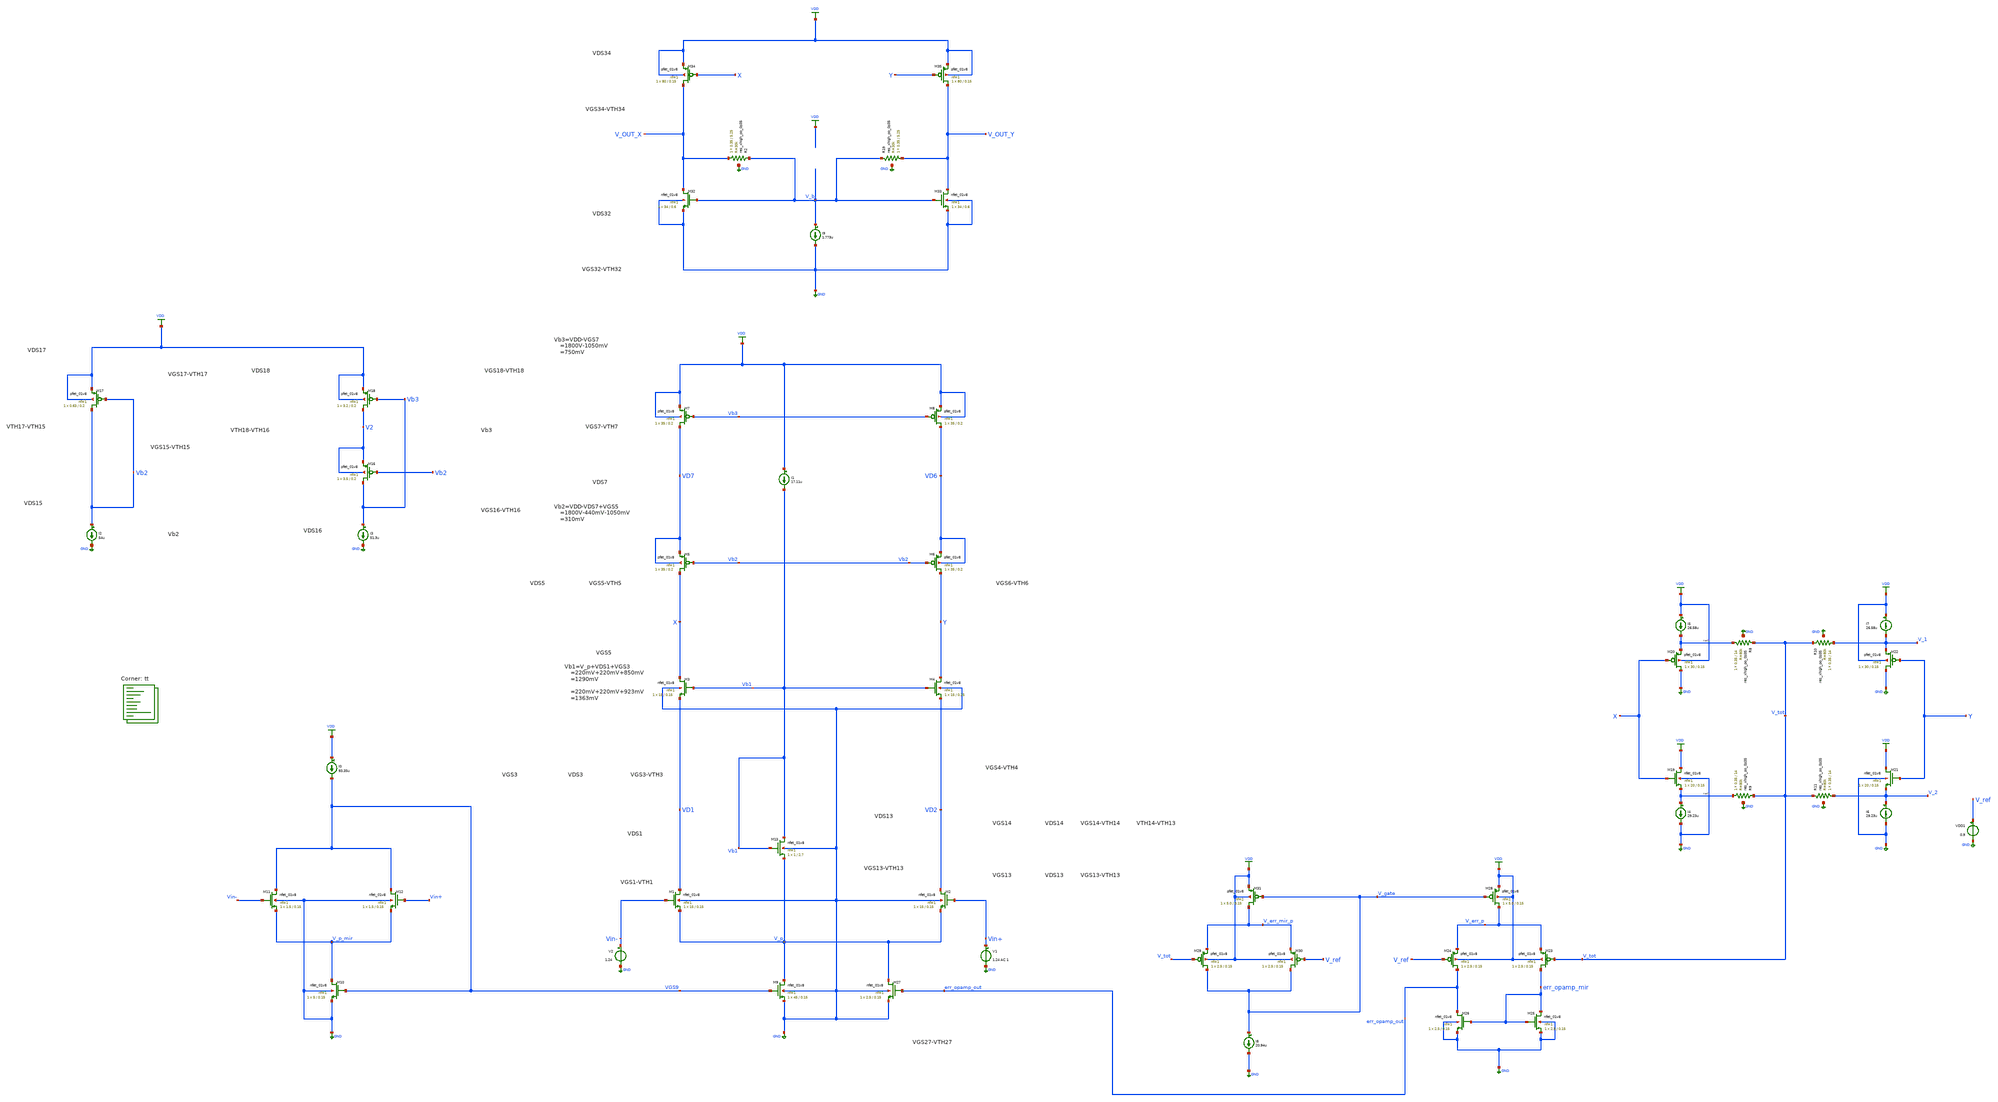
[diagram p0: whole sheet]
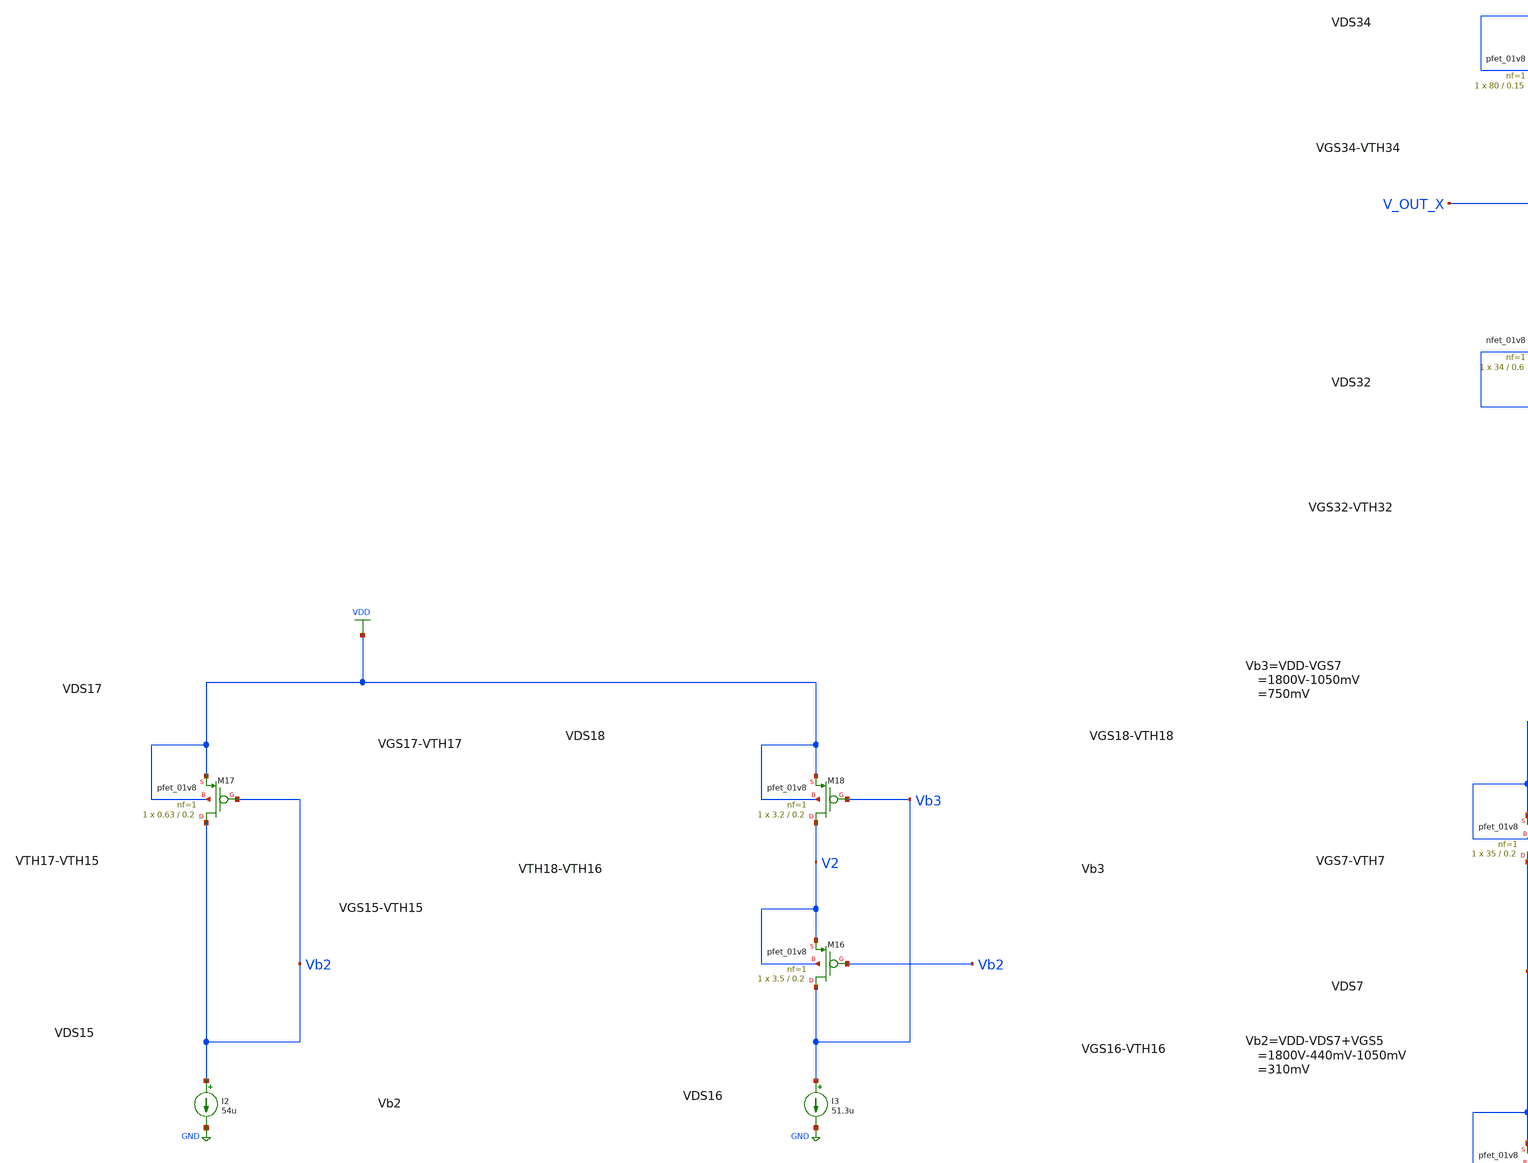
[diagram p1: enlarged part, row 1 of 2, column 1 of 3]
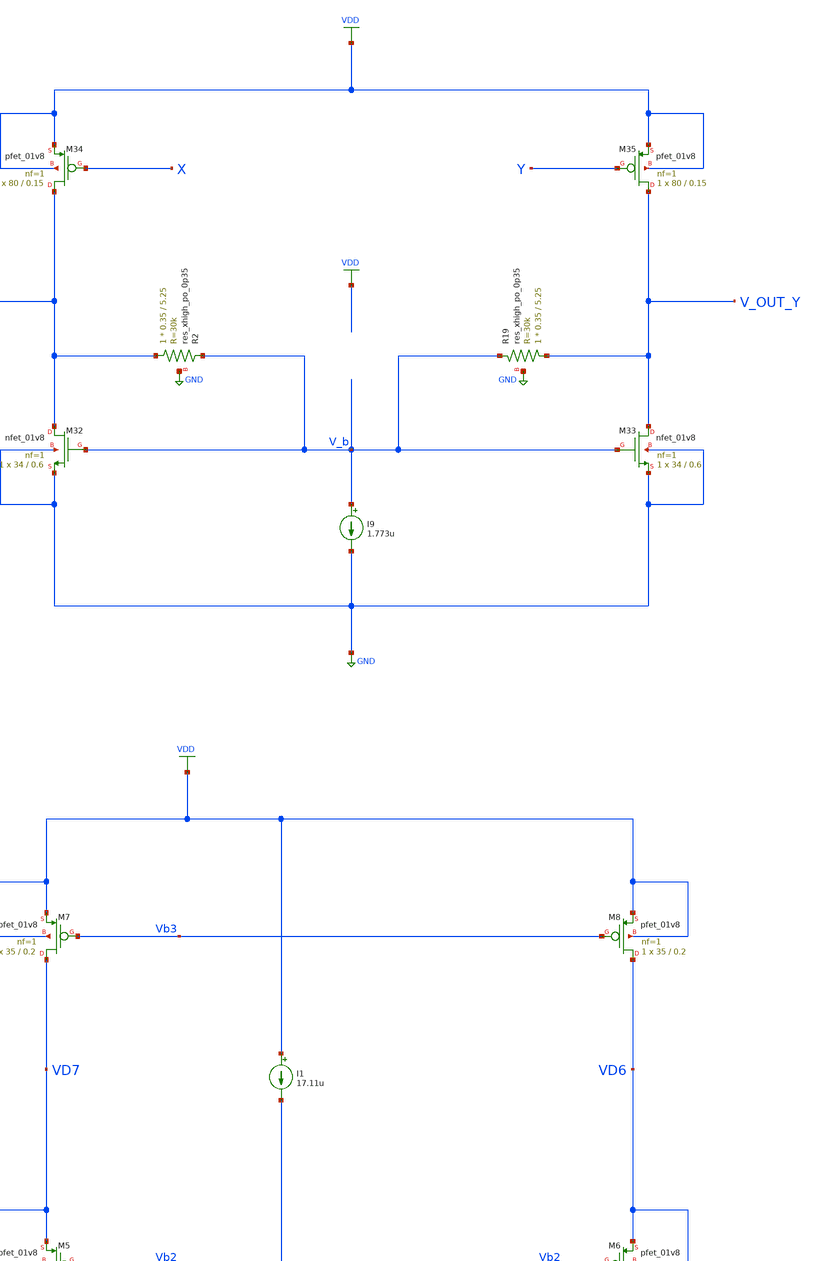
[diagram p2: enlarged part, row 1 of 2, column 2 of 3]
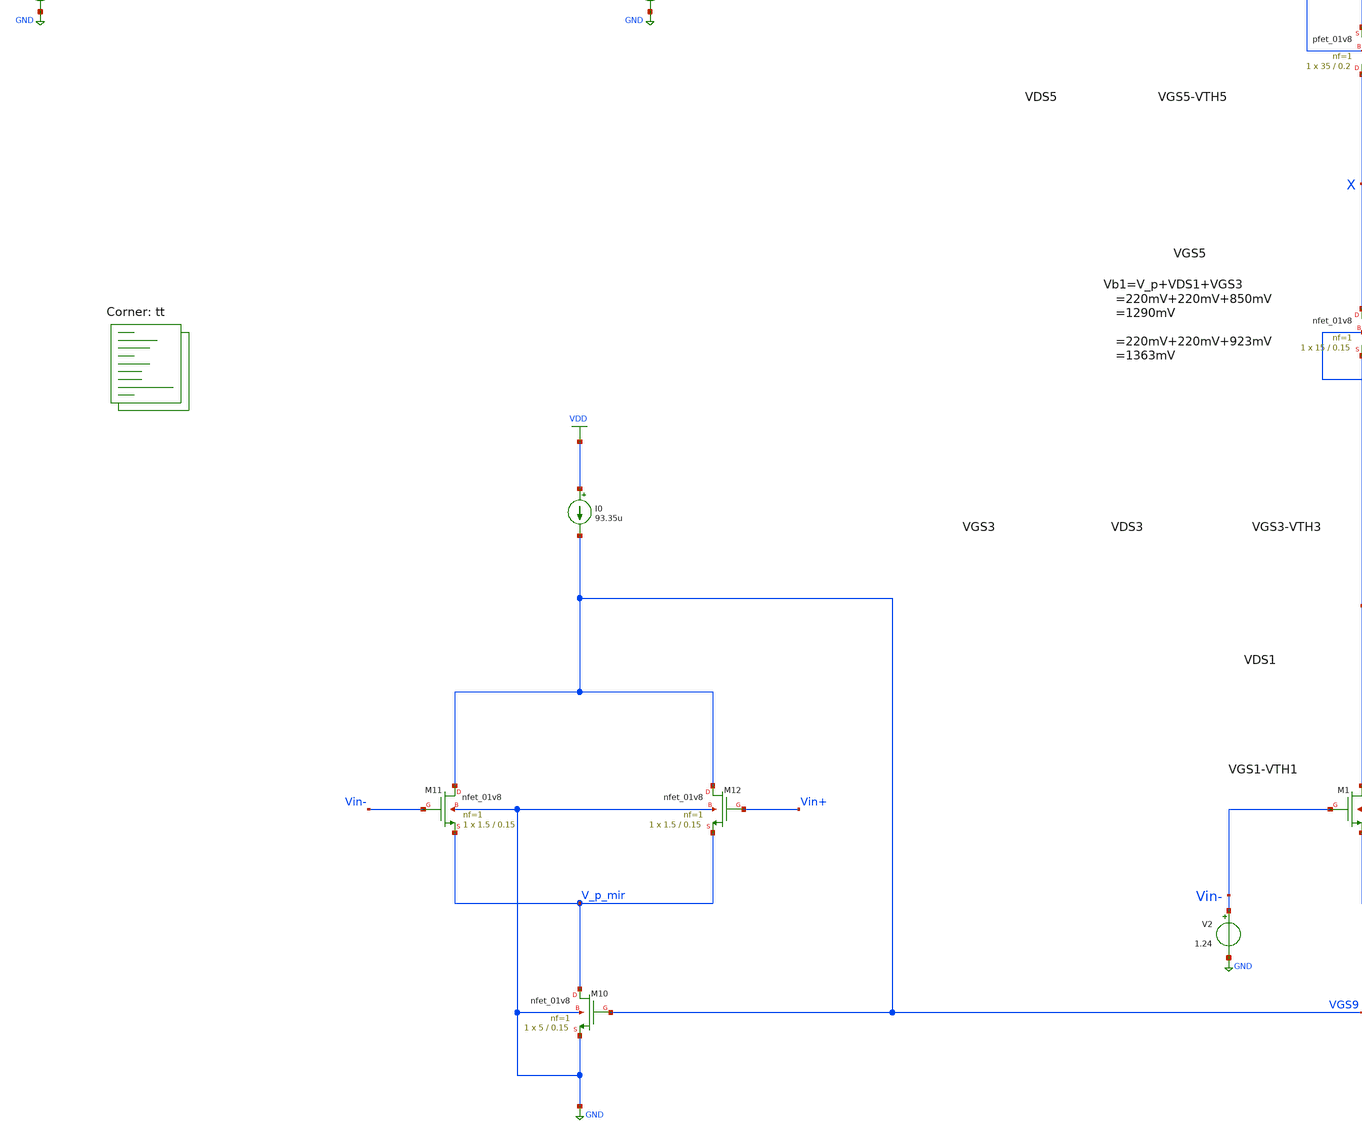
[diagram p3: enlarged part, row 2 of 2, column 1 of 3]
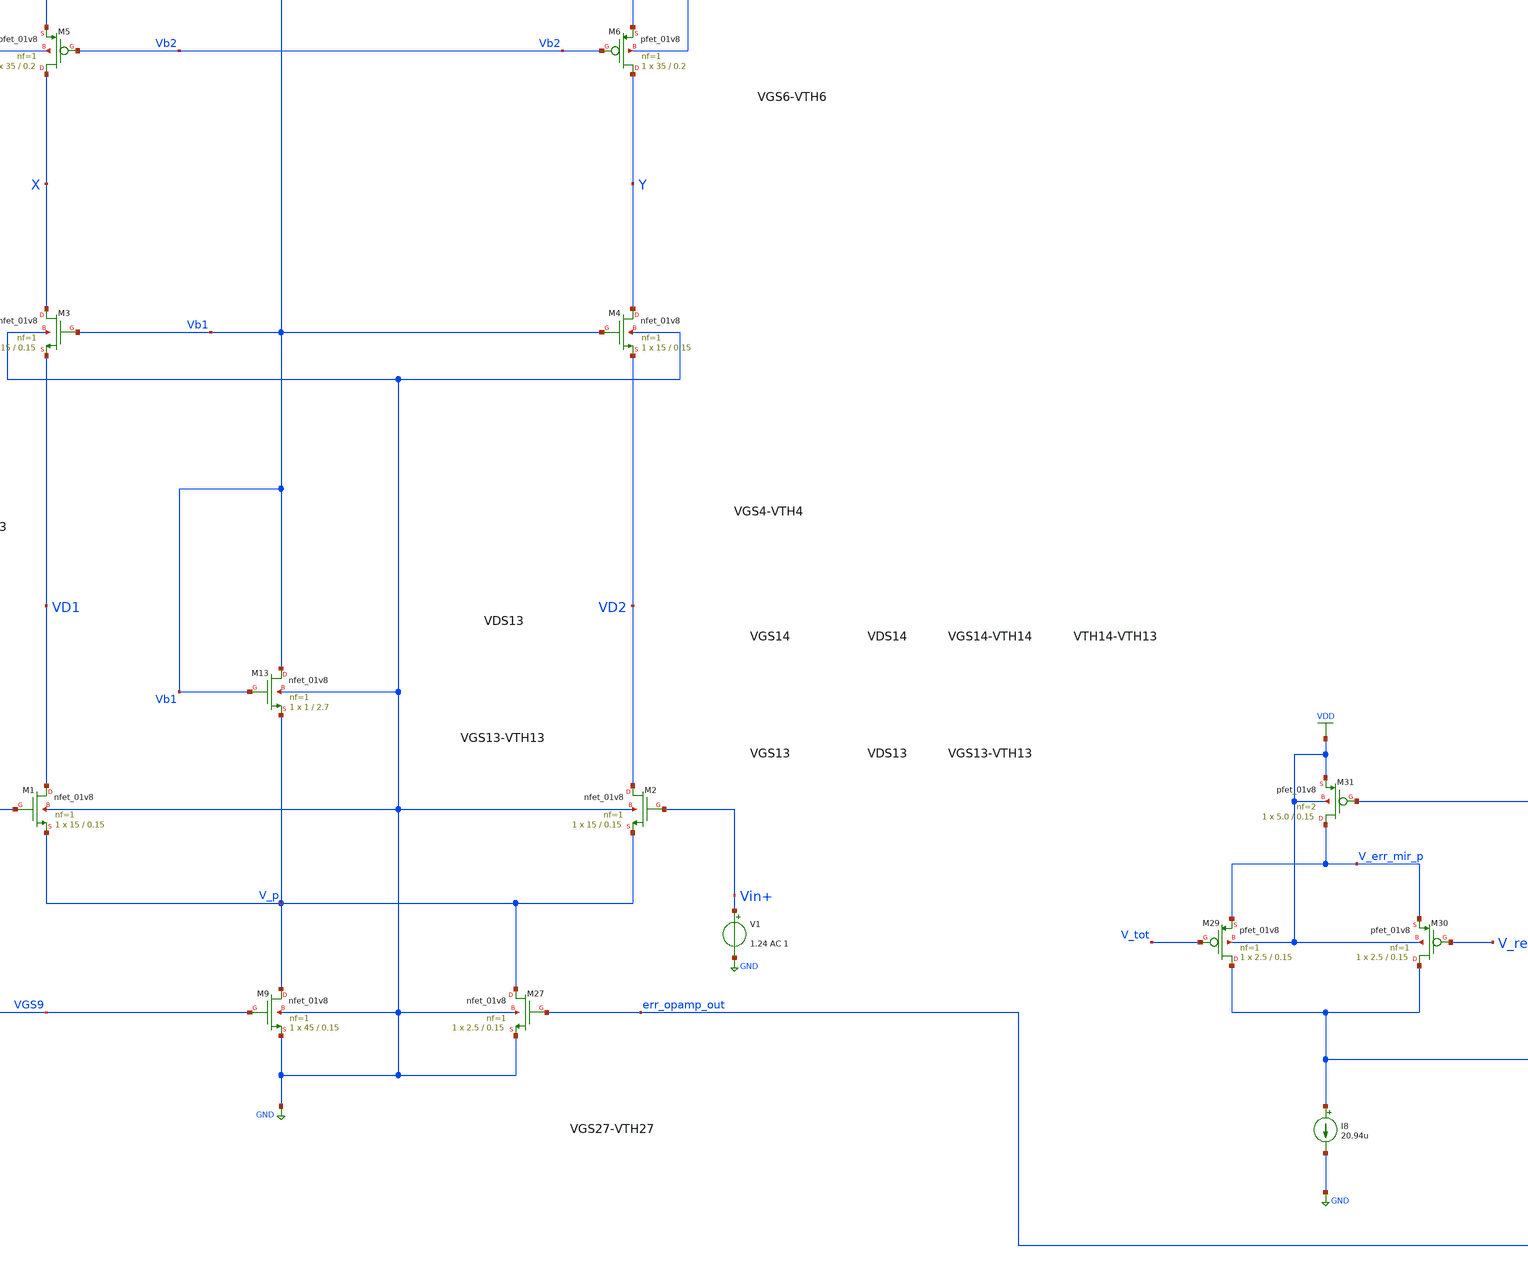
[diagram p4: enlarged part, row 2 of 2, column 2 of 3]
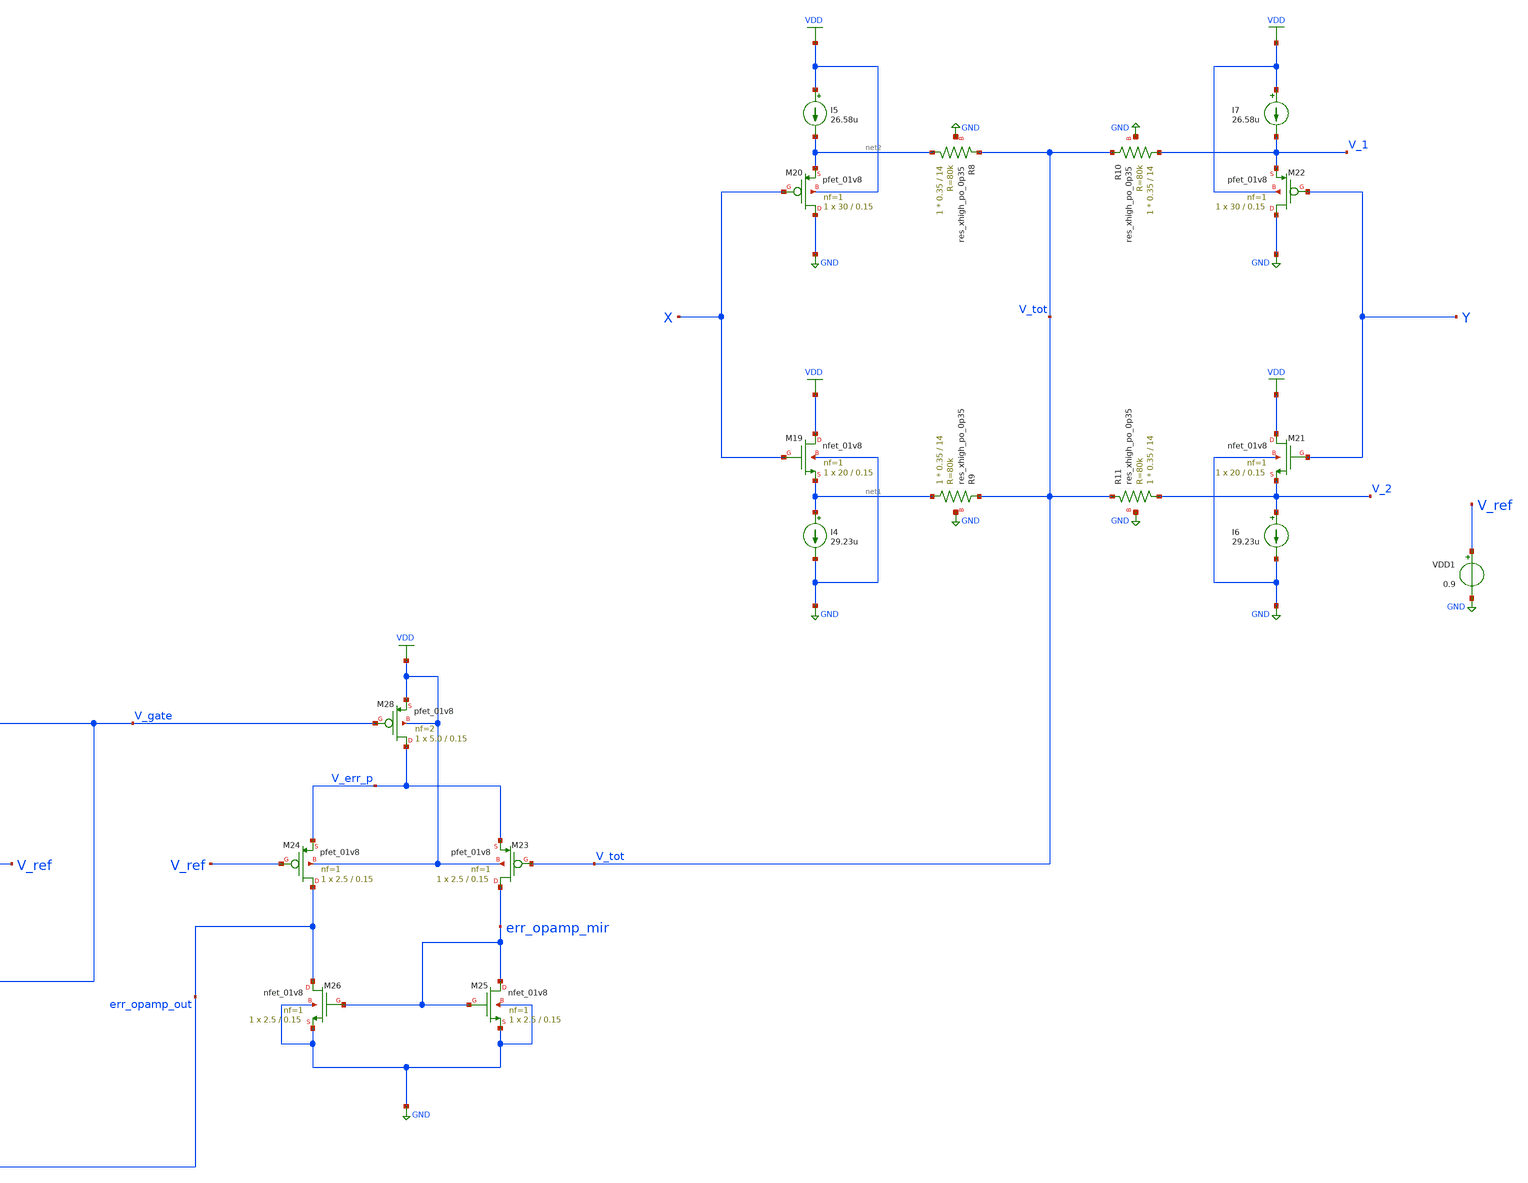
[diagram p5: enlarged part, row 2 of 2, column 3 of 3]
** sch_path: projects/opamp/xschem_ngspice/tb_opamp_1st_stage_4.sch
**.subckt tb_opamp_1st_stage_4
XM1 VD1 Vin- V_p GND sky130_fd_pr__nfet_01v8 L=0.15 W=15 nf=1 ad='int((nf+1)/2) * W/nf * 0.29' as='int((nf+2)/2) * W/nf * 0.29'
+ pd='2*int((nf+1)/2) * (W/nf + 0.29)' ps='2*int((nf+2)/2) * (W/nf + 0.29)' nrd='0.29 / W' nrs='0.29 / W'
+ sa=0 sb=0 sd=0 mult=1 m=1
XM2 VD2 Vin+ V_p GND sky130_fd_pr__nfet_01v8 L=0.15 W=15 nf=1 ad='int((nf+1)/2) * W/nf * 0.29' as='int((nf+2)/2) * W/nf * 0.29'
+ pd='2*int((nf+1)/2) * (W/nf + 0.29)' ps='2*int((nf+2)/2) * (W/nf + 0.29)' nrd='0.29 / W' nrs='0.29 / W'
+ sa=0 sb=0 sd=0 mult=1 m=1
XM3 X Vb1 VD1 GND sky130_fd_pr__nfet_01v8 L=0.15 W=15 nf=1 ad='int((nf+1)/2) * W/nf * 0.29' as='int((nf+2)/2) * W/nf * 0.29'
+ pd='2*int((nf+1)/2) * (W/nf + 0.29)' ps='2*int((nf+2)/2) * (W/nf + 0.29)' nrd='0.29 / W' nrs='0.29 / W'
+ sa=0 sb=0 sd=0 mult=1 m=1
XM4 Y Vb1 VD2 GND sky130_fd_pr__nfet_01v8 L=0.15 W=15 nf=1 ad='int((nf+1)/2) * W/nf * 0.29' as='int((nf+2)/2) * W/nf * 0.29'
+ pd='2*int((nf+1)/2) * (W/nf + 0.29)' ps='2*int((nf+2)/2) * (W/nf + 0.29)' nrd='0.29 / W' nrs='0.29 / W'
+ sa=0 sb=0 sd=0 mult=1 m=1
XM5 X Vb2 VD7 VD7 sky130_fd_pr__pfet_01v8 L=0.2 W=35 nf=1 ad='int((nf+1)/2) * W/nf * 0.29' as='int((nf+2)/2) * W/nf * 0.29'
+ pd='2*int((nf+1)/2) * (W/nf + 0.29)' ps='2*int((nf+2)/2) * (W/nf + 0.29)' nrd='0.29 / W' nrs='0.29 / W'
+ sa=0 sb=0 sd=0 mult=1 m=1
XM6 Y Vb2 VD6 VD6 sky130_fd_pr__pfet_01v8 L=0.2 W=35 nf=1 ad='int((nf+1)/2) * W/nf * 0.29' as='int((nf+2)/2) * W/nf * 0.29'
+ pd='2*int((nf+1)/2) * (W/nf + 0.29)' ps='2*int((nf+2)/2) * (W/nf + 0.29)' nrd='0.29 / W' nrs='0.29 / W'
+ sa=0 sb=0 sd=0 mult=1 m=1
XM7 VD7 Vb3 VDD VDD sky130_fd_pr__pfet_01v8 L=0.2 W=35 nf=1 ad='int((nf+1)/2) * W/nf * 0.29' as='int((nf+2)/2) * W/nf * 0.29'
+ pd='2*int((nf+1)/2) * (W/nf + 0.29)' ps='2*int((nf+2)/2) * (W/nf + 0.29)' nrd='0.29 / W' nrs='0.29 / W'
+ sa=0 sb=0 sd=0 mult=1 m=1
XM8 VD6 Vb3 VDD VDD sky130_fd_pr__pfet_01v8 L=0.2 W=35 nf=1 ad='int((nf+1)/2) * W/nf * 0.29' as='int((nf+2)/2) * W/nf * 0.29'
+ pd='2*int((nf+1)/2) * (W/nf + 0.29)' ps='2*int((nf+2)/2) * (W/nf + 0.29)' nrd='0.29 / W' nrs='0.29 / W'
+ sa=0 sb=0 sd=0 mult=1 m=1
XM9 V_p VGS9 GND GND sky130_fd_pr__nfet_01v8 L=0.15 W=45 nf=1 ad='int((nf+1)/2) * W/nf * 0.29' as='int((nf+2)/2) * W/nf * 0.29'
+ pd='2*int((nf+1)/2) * (W/nf + 0.29)' ps='2*int((nf+2)/2) * (W/nf + 0.29)' nrd='0.29 / W' nrs='0.29 / W'
+ sa=0 sb=0 sd=0 mult=1 m=1
XM10 V_p_mir VGS9 GND GND sky130_fd_pr__nfet_01v8 L=0.15 W=5 nf=1 ad='int((nf+1)/2) * W/nf * 0.29' as='int((nf+2)/2) * W/nf * 0.29'
+ pd='2*int((nf+1)/2) * (W/nf + 0.29)' ps='2*int((nf+2)/2) * (W/nf + 0.29)' nrd='0.29 / W' nrs='0.29 / W'
+ sa=0 sb=0 sd=0 mult=1 m=1
I0 VDD VGS9 93.35u
XM11 VGS9 Vin- V_p_mir GND sky130_fd_pr__nfet_01v8 L=0.15 W=1.5 nf=1 ad='int((nf+1)/2) * W/nf * 0.29'
+ as='int((nf+2)/2) * W/nf * 0.29' pd='2*int((nf+1)/2) * (W/nf + 0.29)' ps='2*int((nf+2)/2) * (W/nf + 0.29)'
+ nrd='0.29 / W' nrs='0.29 / W' sa=0 sb=0 sd=0 mult=1 m=1
XM12 VGS9 Vin+ V_p_mir GND sky130_fd_pr__nfet_01v8 L=0.15 W=1.5 nf=1 ad='int((nf+1)/2) * W/nf * 0.29'
+ as='int((nf+2)/2) * W/nf * 0.29' pd='2*int((nf+1)/2) * (W/nf + 0.29)' ps='2*int((nf+2)/2) * (W/nf + 0.29)'
+ nrd='0.29 / W' nrs='0.29 / W' sa=0 sb=0 sd=0 mult=1 m=1
XM13 Vb1 Vb1 V_p GND sky130_fd_pr__nfet_01v8 L=2.7 W=1 nf=1 ad='int((nf+1)/2) * W/nf * 0.29' as='int((nf+2)/2) * W/nf * 0.29'
+ pd='2*int((nf+1)/2) * (W/nf + 0.29)' ps='2*int((nf+2)/2) * (W/nf + 0.29)' nrd='0.29 / W' nrs='0.29 / W'
+ sa=0 sb=0 sd=0 mult=1 m=1
I1 VDD Vb1 17.11u
XM16 Vb3 Vb2 V2 V2 sky130_fd_pr__pfet_01v8 L=0.2 W=3.5 nf=1 ad='int((nf+1)/2) * W/nf * 0.29' as='int((nf+2)/2) * W/nf * 0.29'
+ pd='2*int((nf+1)/2) * (W/nf + 0.29)' ps='2*int((nf+2)/2) * (W/nf + 0.29)' nrd='0.29 / W' nrs='0.29 / W'
+ sa=0 sb=0 sd=0 mult=1 m=1
XM17 Vb2 Vb2 VDD VDD sky130_fd_pr__pfet_01v8 L=0.2 W=0.63 nf=1 ad='int((nf+1)/2) * W/nf * 0.29' as='int((nf+2)/2) * W/nf * 0.29'
+ pd='2*int((nf+1)/2) * (W/nf + 0.29)' ps='2*int((nf+2)/2) * (W/nf + 0.29)' nrd='0.29 / W' nrs='0.29 / W'
+ sa=0 sb=0 sd=0 mult=1 m=1
XM18 V2 Vb3 VDD VDD sky130_fd_pr__pfet_01v8 L=0.2 W=3.2 nf=1 ad='int((nf+1)/2) * W/nf * 0.29' as='int((nf+2)/2) * W/nf * 0.29'
+ pd='2*int((nf+1)/2) * (W/nf + 0.29)' ps='2*int((nf+2)/2) * (W/nf + 0.29)' nrd='0.29 / W' nrs='0.29 / W'
+ sa=0 sb=0 sd=0 mult=1 m=1
I2 Vb2 GND 54u
I3 Vb3 GND 51.3u
XM19 VDD X net1 GND sky130_fd_pr__nfet_01v8 L=0.15 W=20 nf=1 ad='int((nf+1)/2) * W/nf * 0.29' as='int((nf+2)/2) * W/nf * 0.29'
+ pd='2*int((nf+1)/2) * (W/nf + 0.29)' ps='2*int((nf+2)/2) * (W/nf + 0.29)' nrd='0.29 / W' nrs='0.29 / W'
+ sa=0 sb=0 sd=0 mult=1 m=1
XM20 GND X net2 VDD sky130_fd_pr__pfet_01v8 L=0.15 W=30 nf=1 ad='int((nf+1)/2) * W/nf * 0.29' as='int((nf+2)/2) * W/nf * 0.29'
+ pd='2*int((nf+1)/2) * (W/nf + 0.29)' ps='2*int((nf+2)/2) * (W/nf + 0.29)' nrd='0.29 / W' nrs='0.29 / W'
+ sa=0 sb=0 sd=0 mult=1 m=1
I4 net1 GND 29.23u
I5 VDD net2 26.58u
XR8 net2 V_tot GND sky130_fd_pr__res_xhigh_po_0p35 L=14 mult=1 m=1
XR9 net1 V_tot GND sky130_fd_pr__res_xhigh_po_0p35 L=14 mult=1 m=1
XR10 V_1 V_tot GND sky130_fd_pr__res_xhigh_po_0p35 L=14 mult=1 m=1
XR11 V_2 V_tot GND sky130_fd_pr__res_xhigh_po_0p35 L=14 mult=1 m=1
XM21 VDD Y V_2 GND sky130_fd_pr__nfet_01v8 L=0.15 W=20 nf=1 ad='int((nf+1)/2) * W/nf * 0.29' as='int((nf+2)/2) * W/nf * 0.29'
+ pd='2*int((nf+1)/2) * (W/nf + 0.29)' ps='2*int((nf+2)/2) * (W/nf + 0.29)' nrd='0.29 / W' nrs='0.29 / W'
+ sa=0 sb=0 sd=0 mult=1 m=1
XM22 GND Y V_1 VDD sky130_fd_pr__pfet_01v8 L=0.15 W=30 nf=1 ad='int((nf+1)/2) * W/nf * 0.29' as='int((nf+2)/2) * W/nf * 0.29'
+ pd='2*int((nf+1)/2) * (W/nf + 0.29)' ps='2*int((nf+2)/2) * (W/nf + 0.29)' nrd='0.29 / W' nrs='0.29 / W'
+ sa=0 sb=0 sd=0 mult=1 m=1
I6 V_2 GND 29.23u
I7 VDD V_1 26.58u
XM23 err_opamp_mir V_tot V_err_p VDD sky130_fd_pr__pfet_01v8 L=0.15 W=2.5 nf=1 ad='int((nf+1)/2) * W/nf * 0.29'
+ as='int((nf+2)/2) * W/nf * 0.29' pd='2*int((nf+1)/2) * (W/nf + 0.29)' ps='2*int((nf+2)/2) * (W/nf + 0.29)'
+ nrd='0.29 / W' nrs='0.29 / W' sa=0 sb=0 sd=0 mult=1 m=1
XM24 err_opamp_out V_ref V_err_p VDD sky130_fd_pr__pfet_01v8 L=0.15 W=2.5 nf=1 ad='int((nf+1)/2) * W/nf * 0.29'
+ as='int((nf+2)/2) * W/nf * 0.29' pd='2*int((nf+1)/2) * (W/nf + 0.29)' ps='2*int((nf+2)/2) * (W/nf + 0.29)'
+ nrd='0.29 / W' nrs='0.29 / W' sa=0 sb=0 sd=0 mult=1 m=1
I8 V_gate GND 20.94u
XM25 err_opamp_mir err_opamp_mir GND GND sky130_fd_pr__nfet_01v8 L=0.15 W=2.5 nf=1 ad='int((nf+1)/2) * W/nf * 0.29'
+ as='int((nf+2)/2) * W/nf * 0.29' pd='2*int((nf+1)/2) * (W/nf + 0.29)' ps='2*int((nf+2)/2) * (W/nf + 0.29)'
+ nrd='0.29 / W' nrs='0.29 / W' sa=0 sb=0 sd=0 mult=1 m=1
XM26 err_opamp_out err_opamp_mir GND GND sky130_fd_pr__nfet_01v8 L=0.15 W=2.5 nf=1 ad='int((nf+1)/2) * W/nf * 0.29'
+ as='int((nf+2)/2) * W/nf * 0.29' pd='2*int((nf+1)/2) * (W/nf + 0.29)' ps='2*int((nf+2)/2) * (W/nf + 0.29)'
+ nrd='0.29 / W' nrs='0.29 / W' sa=0 sb=0 sd=0 mult=1 m=1
VDD1 V_ref GND 0.9
XM28 V_err_p V_gate VDD VDD sky130_fd_pr__pfet_01v8 L=0.15 W=5.0 nf=2 ad='int((nf+1)/2) * W/nf * 0.29'
+ as='int((nf+2)/2) * W/nf * 0.29' pd='2*int((nf+1)/2) * (W/nf + 0.29)' ps='2*int((nf+2)/2) * (W/nf + 0.29)'
+ nrd='0.29 / W' nrs='0.29 / W' sa=0 sb=0 sd=0 mult=1 m=1
XM29 V_gate V_tot V_err_mir_p VDD sky130_fd_pr__pfet_01v8 L=0.15 W=2.5 nf=1 ad='int((nf+1)/2) * W/nf * 0.29'
+ as='int((nf+2)/2) * W/nf * 0.29' pd='2*int((nf+1)/2) * (W/nf + 0.29)' ps='2*int((nf+2)/2) * (W/nf + 0.29)'
+ nrd='0.29 / W' nrs='0.29 / W' sa=0 sb=0 sd=0 mult=1 m=1
XM30 V_gate V_ref V_err_mir_p VDD sky130_fd_pr__pfet_01v8 L=0.15 W=2.5 nf=1 ad='int((nf+1)/2) * W/nf * 0.29'
+ as='int((nf+2)/2) * W/nf * 0.29' pd='2*int((nf+1)/2) * (W/nf + 0.29)' ps='2*int((nf+2)/2) * (W/nf + 0.29)'
+ nrd='0.29 / W' nrs='0.29 / W' sa=0 sb=0 sd=0 mult=1 m=1
XM31 V_err_mir_p V_gate VDD VDD sky130_fd_pr__pfet_01v8 L=0.15 W=5.0 nf=2 ad='int((nf+1)/2) * W/nf * 0.29'
+ as='int((nf+2)/2) * W/nf * 0.29' pd='2*int((nf+1)/2) * (W/nf + 0.29)' ps='2*int((nf+2)/2) * (W/nf + 0.29)'
+ nrd='0.29 / W' nrs='0.29 / W' sa=0 sb=0 sd=0 mult=1 m=1
V2 Vin- GND 1.24
V1 Vin+ GND 1.24 AC 1
XM32 V_OUT_X V_b GND GND sky130_fd_pr__nfet_01v8 L=0.6 W=34 nf=1 ad='int((nf+1)/2) * W/nf * 0.29' as='int((nf+2)/2) * W/nf * 0.29'
+ pd='2*int((nf+1)/2) * (W/nf + 0.29)' ps='2*int((nf+2)/2) * (W/nf + 0.29)' nrd='0.29 / W' nrs='0.29 / W'
+ sa=0 sb=0 sd=0 mult=1 m=1
XM33 V_OUT_Y V_b GND GND sky130_fd_pr__nfet_01v8 L=0.6 W=34 nf=1 ad='int((nf+1)/2) * W/nf * 0.29' as='int((nf+2)/2) * W/nf * 0.29'
+ pd='2*int((nf+1)/2) * (W/nf + 0.29)' ps='2*int((nf+2)/2) * (W/nf + 0.29)' nrd='0.29 / W' nrs='0.29 / W'
+ sa=0 sb=0 sd=0 mult=1 m=1
XM34 V_OUT_X X VDD VDD sky130_fd_pr__pfet_01v8 L=0.15 W=80 nf=1 ad='int((nf+1)/2) * W/nf * 0.29' as='int((nf+2)/2) * W/nf * 0.29'
+ pd='2*int((nf+1)/2) * (W/nf + 0.29)' ps='2*int((nf+2)/2) * (W/nf + 0.29)' nrd='0.29 / W' nrs='0.29 / W'
+ sa=0 sb=0 sd=0 mult=1 m=1
XM35 V_OUT_Y Y VDD VDD sky130_fd_pr__pfet_01v8 L=0.15 W=80 nf=1 ad='int((nf+1)/2) * W/nf * 0.29' as='int((nf+2)/2) * W/nf * 0.29'
+ pd='2*int((nf+1)/2) * (W/nf + 0.29)' ps='2*int((nf+2)/2) * (W/nf + 0.29)' nrd='0.29 / W' nrs='0.29 / W'
+ sa=0 sb=0 sd=0 mult=1 m=1
XR2 V_OUT_X V_b GND sky130_fd_pr__res_xhigh_po_0p35 L=5.25 mult=1 m=1
XR19 V_OUT_Y V_b GND sky130_fd_pr__res_xhigh_po_0p35 L=5.25 mult=1 m=1
I9 V_b GND 1.773u
XM27 V_p err_opamp_out GND GND sky130_fd_pr__nfet_01v8 L=0.15 W=2.5 nf=1 ad='int((nf+1)/2) * W/nf * 0.29'
+ as='int((nf+2)/2) * W/nf * 0.29' pd='2*int((nf+1)/2) * (W/nf + 0.29)' ps='2*int((nf+2)/2) * (W/nf + 0.29)'
+ nrd='0.29 / W' nrs='0.29 / W' sa=0 sb=0 sd=0 mult=1 m=1
**** begin user architecture code



.option method=gear
.option wnflag=1
.option savecurrents

.save @m.xm1.msky130_fd_pr__nfet_01v8[gm] @m.xm1.msky130_fd_pr__nfet_01v8[vth] @m.xm2.msky130_fd_pr__nfet_01v8[gm] @m.xm2.msky130_fd_pr__nfet_01v8[vth] @m.xm3.msky130_fd_pr__nfet_01v8[gm] @m.xm3.msky130_fd_pr__nfet_01v8[vth] @m.xm4.msky130_fd_pr__nfet_01v8[gm] @m.xm4.msky130_fd_pr__nfet_01v8[vth] @m.xm5.msky130_fd_pr__pfet_01v8[gm] @m.xm5.msky130_fd_pr__pfet_01v8[vth] @m.xm6.msky130_fd_pr__pfet_01v8[gm] @m.xm6.msky130_fd_pr__pfet_01v8[vth] @m.xm7.msky130_fd_pr__pfet_01v8[gm] @m.xm7.msky130_fd_pr__pfet_01v8[vth] @m.xm8.msky130_fd_pr__pfet_01v8[gm] @m.xm8.msky130_fd_pr__pfet_01v8[vth] @m.xm9.msky130_fd_pr__nfet_01v8[gm] @m.xm9.msky130_fd_pr__nfet_01v8[vth] @m.xm10.msky130_fd_pr__nfet_01v8[gm] @m.xm10.msky130_fd_pr__nfet_01v8[vth] @m.xm11.msky130_fd_pr__nfet_01v8[gm] @m.xm11.msky130_fd_pr__nfet_01v8[vth] @m.xm12.msky130_fd_pr__nfet_01v8[gm] @m.xm12.msky130_fd_pr__nfet_01v8[vth] @m.xm13.msky130_fd_pr__nfet_01v8[gm] @m.xm13.msky130_fd_pr__nfet_01v8[vth] @m.xm14.msky130_fd_pr__nfet_01v8[gm] @m.xm14.msky130_fd_pr__nfet_01v8[vth] @m.xm15.msky130_fd_pr__pfet_01v8[gm] @m.xm15.msky130_fd_pr__pfet_01v8[vth] @m.xm16.msky130_fd_pr__pfet_01v8[gm] @m.xm16.msky130_fd_pr__pfet_01v8[vth] @m.xm17.msky130_fd_pr__pfet_01v8[gm] @m.xm17.msky130_fd_pr__pfet_01v8[vth] @m.xm18.msky130_fd_pr__pfet_01v8[gm] @m.xm18.msky130_fd_pr__pfet_01v8[vth] @m.xm19.msky130_fd_pr__nfet_01v8[gm] @m.xm19.msky130_fd_pr__nfet_01v8[vth] @m.xm20.msky130_fd_pr__pfet_01v8[gm] @m.xm20.msky130_fd_pr__pfet_01v8[vth] @m.xm21.msky130_fd_pr__nfet_01v8[gm] @m.xm21.msky130_fd_pr__nfet_01v8[vth] @m.xm22.msky130_fd_pr__pfet_01v8[gm] @m.xm22.msky130_fd_pr__pfet_01v8[vth] @m.xm23.msky130_fd_pr__pfet_01v8[gm] @m.xm23.msky130_fd_pr__pfet_01v8[vth] @m.xm24.msky130_fd_pr__pfet_01v8[gm] @m.xm24.msky130_fd_pr__pfet_01v8[vth] @m.xm25.msky130_fd_pr__nfet_01v8[gm] @m.xm25.msky130_fd_pr__nfet_01v8[vth] @m.xm26.msky130_fd_pr__nfet_01v8[gm] @m.xm26.msky130_fd_pr__nfet_01v8[vth] @m.xm27.msky130_fd_pr__nfet_01v8[gm] @m.xm27.msky130_fd_pr__nfet_01v8[vth] @m.xm28.msky130_fd_pr__nfet_01v8[gm] @m.xm28.msky130_fd_pr__nfet_01v8[vth] @m.xm29.msky130_fd_pr__nfet_01v8[gm] @m.xm29.msky130_fd_pr__nfet_01v8[vth] @m.xm30.msky130_fd_pr__nfet_01v8[gm] @m.xm30.msky130_fd_pr__nfet_01v8[vth] @m.xm31.msky130_fd_pr__nfet_01v8[gm] @m.xm31.msky130_fd_pr__nfet_01v8[vth] @m.xm32.msky130_fd_pr__nfet_01v8[gm] @m.xm32.msky130_fd_pr__nfet_01v8[vth] @m.xm33.msky130_fd_pr__nfet_01v8[gm] @m.xm33.msky130_fd_pr__nfet_01v8[vth] @m.xm34.msky130_fd_pr__pfet_01v8[gm] @m.xm34.msky130_fd_pr__pfet_01v8[vth] @m.xm35.msky130_fd_pr__pfet_01v8[gm] @m.xm35.msky130_fd_pr__pfet_01v8[vth]

.ic v(v_top) = 1.8

.control

  save all
  * dc V1 1.2 1.28 0.001
  * dc VDD 0 1.8 0.9
  * tran 0.4u 3m
  * tran 0.4n 3u
  * tran 1n 12u
  ac dec 20 1 1T
  remzerovec
  write tb_opamp_1st_stage_4.raw
  set appendwrite
  let first_out = x - y
  let second_out = v_out_x - v_out_y

.endc




.lib $::SKYWATER_MODELS/sky130.lib.spice tt
**** end user architecture code
**.ends
.GLOBAL VDD
.GLOBAL GND
.end
